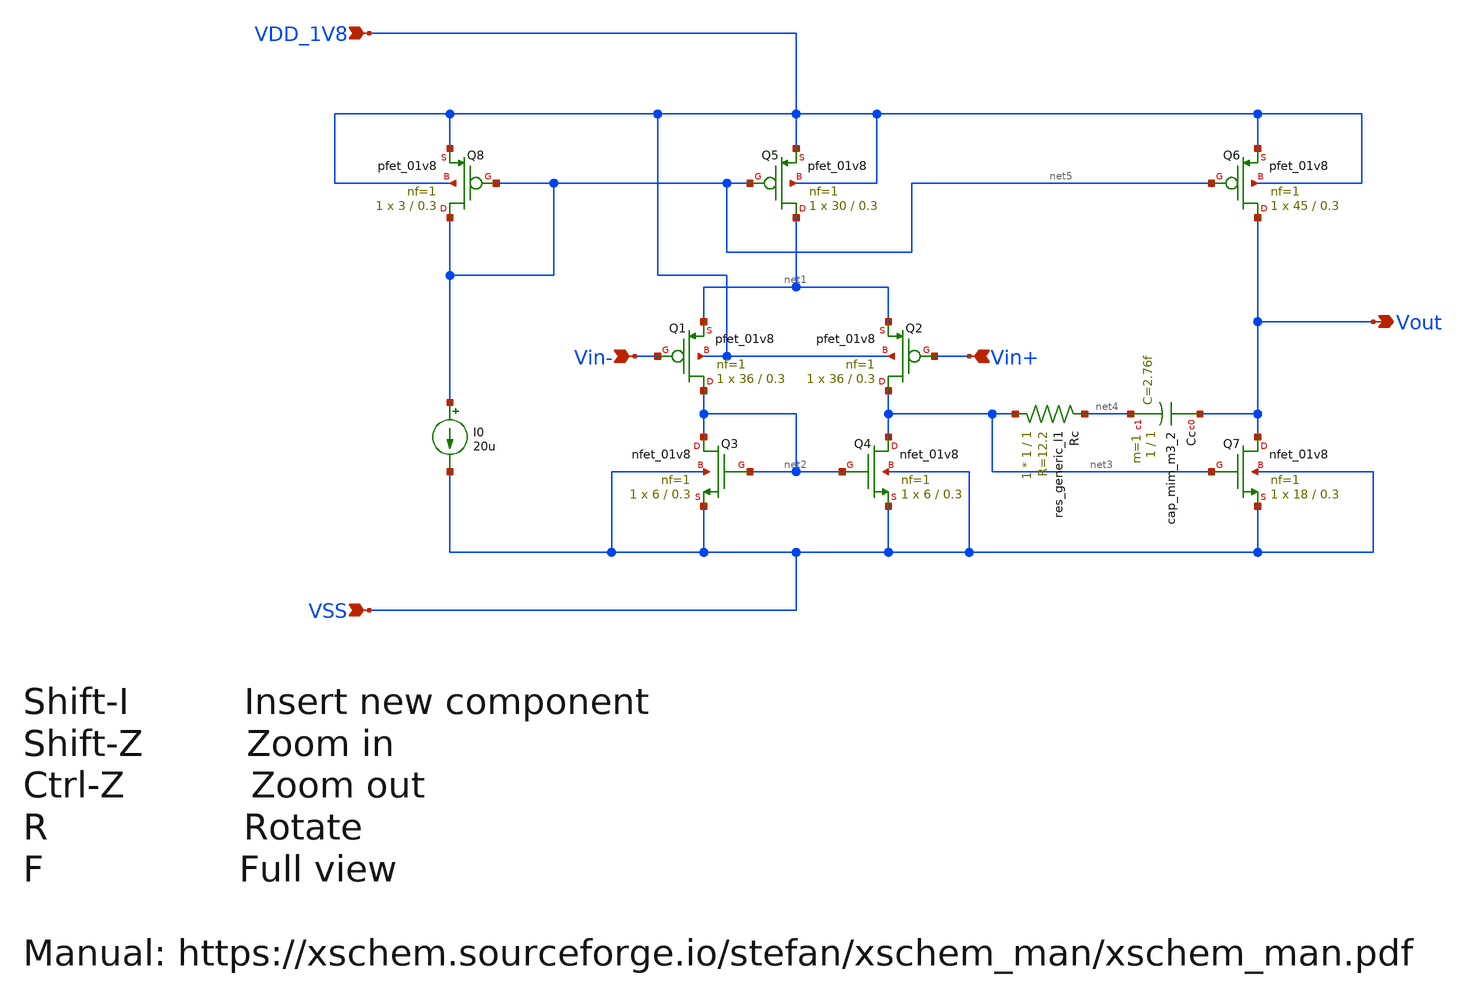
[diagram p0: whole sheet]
** sch_path: rply_mainopamp_sky130nm/design/RPLY_MAINOPAMP_SKY130NM/RPLY_MAINOPAMP.sch
**.subckt RPLY_MAINOPAMP VDD_1V8 VSS Vout Vin- Vin+
*.ipin VDD_1V8
*.ipin VSS
*.opin Vout
*.ipin Vin-
*.ipin Vin+
XQ8 net5 net5 VDD_1V8 VDD_1V8 sky130_fd_pr__pfet_01v8 L=0.3 W=3 nf=1 ad='int((nf+1)/2) * W/nf * 0.29'
+ as='int((nf+2)/2) * W/nf * 0.29' pd='2*int((nf+1)/2) * (W/nf + 0.29)' ps='2*int((nf+2)/2) * (W/nf + 0.29)'
+ nrd='0.29 / W' nrs='0.29 / W' sa=0 sb=0 sd=0 mult=1 m=1
XQ5 net1 net5 VDD_1V8 VDD_1V8 sky130_fd_pr__pfet_01v8 L=0.3 W=30 nf=1 ad='int((nf+1)/2) * W/nf * 0.29'
+ as='int((nf+2)/2) * W/nf * 0.29' pd='2*int((nf+1)/2) * (W/nf + 0.29)' ps='2*int((nf+2)/2) * (W/nf + 0.29)'
+ nrd='0.29 / W' nrs='0.29 / W' sa=0 sb=0 sd=0 mult=1 m=1
XQ6 Vout net5 VDD_1V8 VDD_1V8 sky130_fd_pr__pfet_01v8 L=0.3 W=45 nf=1 ad='int((nf+1)/2) * W/nf * 0.29'
+ as='int((nf+2)/2) * W/nf * 0.29' pd='2*int((nf+1)/2) * (W/nf + 0.29)' ps='2*int((nf+2)/2) * (W/nf + 0.29)'
+ nrd='0.29 / W' nrs='0.29 / W' sa=0 sb=0 sd=0 mult=1 m=1
XQ1 net2 Vin- net1 VDD_1V8 sky130_fd_pr__pfet_01v8 L=0.3 W=36 nf=1 ad='int((nf+1)/2) * W/nf * 0.29' as='int((nf+2)/2) * W/nf * 0.29'
+ pd='2*int((nf+1)/2) * (W/nf + 0.29)' ps='2*int((nf+2)/2) * (W/nf + 0.29)' nrd='0.29 / W' nrs='0.29 / W'
+ sa=0 sb=0 sd=0 mult=1 m=1
XQ2 net3 Vin+ net1 VDD_1V8 sky130_fd_pr__pfet_01v8 L=0.3 W=36 nf=1 ad='int((nf+1)/2) * W/nf * 0.29' as='int((nf+2)/2) * W/nf * 0.29'
+ pd='2*int((nf+1)/2) * (W/nf + 0.29)' ps='2*int((nf+2)/2) * (W/nf + 0.29)' nrd='0.29 / W' nrs='0.29 / W'
+ sa=0 sb=0 sd=0 mult=1 m=1
XQ4 net3 net2 VSS VSS sky130_fd_pr__nfet_01v8 L=0.3 W=6 nf=1 ad='int((nf+1)/2) * W/nf * 0.29' as='int((nf+2)/2) * W/nf * 0.29'
+ pd='2*int((nf+1)/2) * (W/nf + 0.29)' ps='2*int((nf+2)/2) * (W/nf + 0.29)' nrd='0.29 / W' nrs='0.29 / W'
+ sa=0 sb=0 sd=0 mult=1 m=1
XQ3 net2 net2 VSS VSS sky130_fd_pr__nfet_01v8 L=0.3 W=6 nf=1 ad='int((nf+1)/2) * W/nf * 0.29' as='int((nf+2)/2) * W/nf * 0.29'
+ pd='2*int((nf+1)/2) * (W/nf + 0.29)' ps='2*int((nf+2)/2) * (W/nf + 0.29)' nrd='0.29 / W' nrs='0.29 / W'
+ sa=0 sb=0 sd=0 mult=1 m=1
XQ7 Vout net3 VSS VSS sky130_fd_pr__nfet_01v8 L=0.3 W=18 nf=1 ad='int((nf+1)/2) * W/nf * 0.29' as='int((nf+2)/2) * W/nf * 0.29'
+ pd='2*int((nf+1)/2) * (W/nf + 0.29)' ps='2*int((nf+2)/2) * (W/nf + 0.29)' nrd='0.29 / W' nrs='0.29 / W'
+ sa=0 sb=0 sd=0 mult=1 m=1
XCc Vout net4 sky130_fd_pr__cap_mim_m3_2 W=1 L=1 MF=1 m=1
Rc net3 net4 sky130_fd_pr__res_generic_l1 W=1 L=1 m=1
I0 net5 VSS 20u
**.ends
.end
